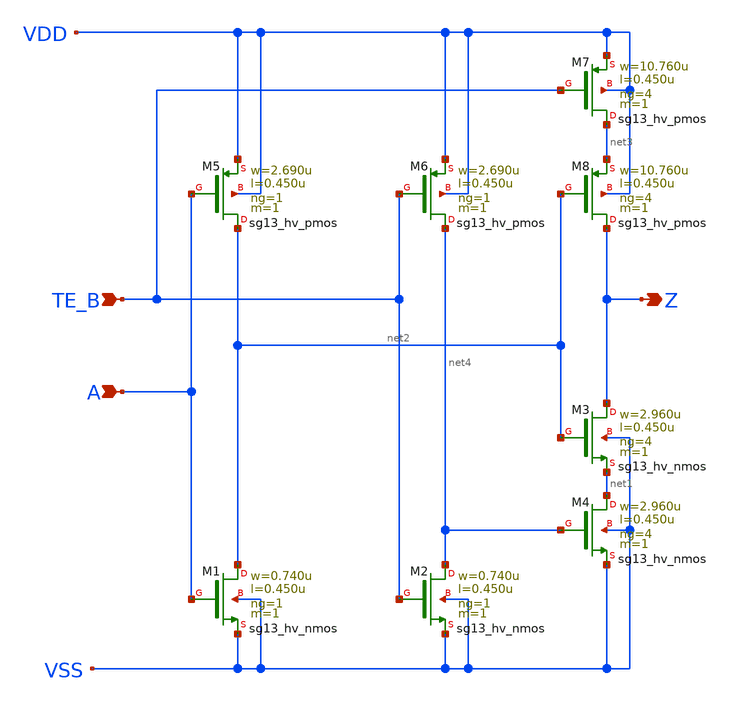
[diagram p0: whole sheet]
** sch_path: ihp-sg13g2/libs.ref/sg13g2_stdcell_hv/sch/xschem/sg13g2_hv_ebufn_4.sch
* Copyright 2023 IHP PDK Authors
* Licensed under the Apache License, Version 2.0 (the "License");
* you may not use this file except in compliance with the License.
* You may obtain a copy of the License at
* https://www.apache.org/licenses/LICENSE-2.0
* Unless required by applicable law or agreed to in writing, software
* distributed under the License is distributed on an "AS IS" BASIS,
* WITHOUT WARRANTIES OR CONDITIONS OF ANY KIND, either express or implied.
* See the License for the specific language governing permissions and
* limitations under the License.
**.subckt sg13g2_hv_ebufn_4 A TE_B Z
*.ipin A
*.ipin TE_B
*.opin Z
XM1 net2 A VSS VSS sg13_hv_nmos w=0.740u l=0.450u ng=1 m=1 mm_ok=1
XM2 net4 TE_B VSS VSS sg13_hv_nmos w=0.740u l=0.450u ng=1 m=1 mm_ok=1
XM3 Z net2 net1 VSS sg13_hv_nmos w=2.960u l=0.450u ng=4 m=1 mm_ok=1
XM4 net1 net4 VSS VSS sg13_hv_nmos w=2.960u l=0.450u ng=4 m=1 mm_ok=1
XM5 net2 A VDD VDD sg13_hv_pmos w=2.690u l=0.450u ng=1 m=1 mm_ok=1
XM6 net4 TE_B VDD VDD sg13_hv_pmos w=2.690u l=0.450u ng=1 m=1 mm_ok=1
XM7 net3 TE_B VDD VDD sg13_hv_pmos w=10.760u l=0.450u ng=4 m=1 mm_ok=1
XM8 Z net2 net3 VDD sg13_hv_pmos w=10.760u l=0.450u ng=4 m=1 mm_ok=1
**.ends
.end
